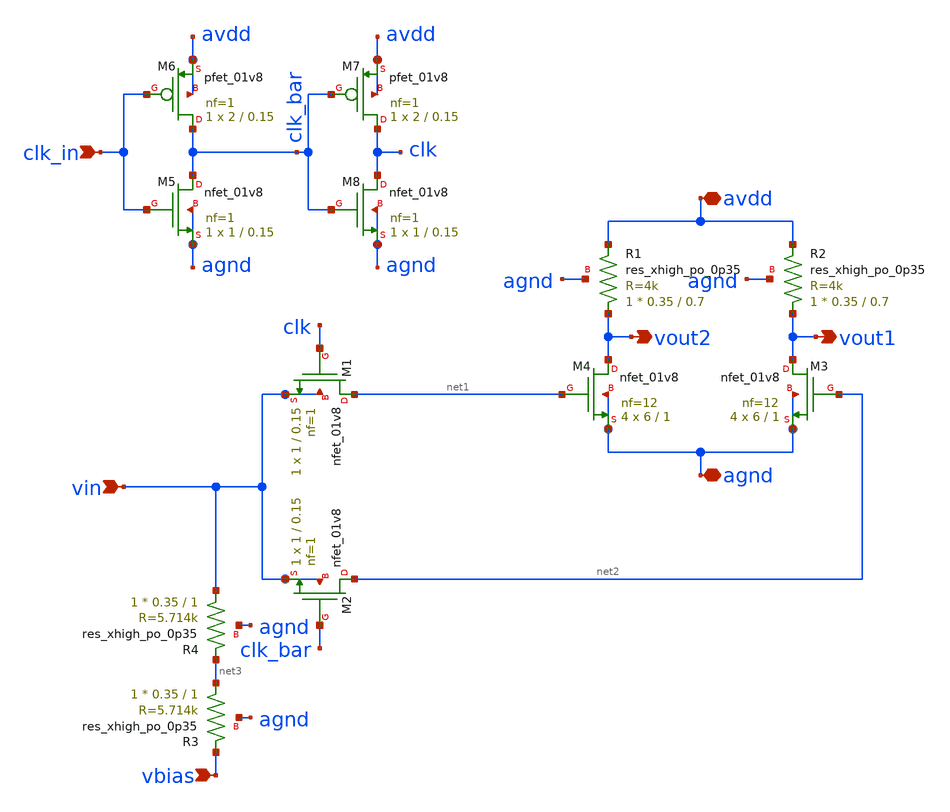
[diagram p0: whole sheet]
** sch_path: Mixer/Mixer.sch
**.subckt Mixer vin clk_in avdd agnd vout2 vout1 vbias
*.ipin vin
*.ipin clk_in
*.iopin avdd
*.iopin agnd
*.opin vout2
*.opin vout1
*.ipin vbias
XM1 net1 clk vin vin sky130_fd_pr__nfet_01v8 L=0.15 W=1 nf=1 ad='int((nf+1)/2) * W/nf * 0.29' as='int((nf+2)/2) * W/nf * 0.29'
+ pd='2*int((nf+1)/2) * (W/nf + 0.29)' ps='2*int((nf+2)/2) * (W/nf + 0.29)' nrd='0.29 / W' nrs='0.29 / W'
+ sa=0 sb=0 sd=0 mult=1 m=1
XM2 net2 clk_bar vin vin sky130_fd_pr__nfet_01v8 L=0.15 W=1 nf=1 ad='int((nf+1)/2) * W/nf * 0.29' as='int((nf+2)/2) * W/nf * 0.29'
+ pd='2*int((nf+1)/2) * (W/nf + 0.29)' ps='2*int((nf+2)/2) * (W/nf + 0.29)' nrd='0.29 / W' nrs='0.29 / W'
+ sa=0 sb=0 sd=0 mult=1 m=1
XM3 vout1 net2 agnd agnd sky130_fd_pr__nfet_01v8 L=1 W=6 nf=12 ad='int((nf+1)/2) * W/nf * 0.29' as='int((nf+2)/2) * W/nf * 0.29'
+ pd='2*int((nf+1)/2) * (W/nf + 0.29)' ps='2*int((nf+2)/2) * (W/nf + 0.29)' nrd='0.29 / W' nrs='0.29 / W'
+ sa=0 sb=0 sd=0 mult=4 m=4
XM4 vout2 net1 agnd agnd sky130_fd_pr__nfet_01v8 L=1 W=6 nf=12 ad='int((nf+1)/2) * W/nf * 0.29' as='int((nf+2)/2) * W/nf * 0.29'
+ pd='2*int((nf+1)/2) * (W/nf + 0.29)' ps='2*int((nf+2)/2) * (W/nf + 0.29)' nrd='0.29 / W' nrs='0.29 / W'
+ sa=0 sb=0 sd=0 mult=4 m=4
XR1 vout2 avdd agnd sky130_fd_pr__res_xhigh_po_0p35 L=0.7 mult=1 m=1
XR2 vout1 avdd agnd sky130_fd_pr__res_xhigh_po_0p35 L=0.7 mult=1 m=1
XR3 net3 vbias agnd sky130_fd_pr__res_xhigh_po_0p35 L=1 mult=1 m=1
XM6 clk_bar clk_in avdd avdd sky130_fd_pr__pfet_01v8 L=0.15 W=2 nf=1 ad='int((nf+1)/2) * W/nf * 0.29'
+ as='int((nf+2)/2) * W/nf * 0.29' pd='2*int((nf+1)/2) * (W/nf + 0.29)' ps='2*int((nf+2)/2) * (W/nf + 0.29)'
+ nrd='0.29 / W' nrs='0.29 / W' sa=0 sb=0 sd=0 mult=1 m=1
XM5 clk_bar clk_in agnd agnd sky130_fd_pr__nfet_01v8 L=0.15 W=1 nf=1 ad='int((nf+1)/2) * W/nf * 0.29'
+ as='int((nf+2)/2) * W/nf * 0.29' pd='2*int((nf+1)/2) * (W/nf + 0.29)' ps='2*int((nf+2)/2) * (W/nf + 0.29)'
+ nrd='0.29 / W' nrs='0.29 / W' sa=0 sb=0 sd=0 mult=1 m=1
XM7 clk clk_bar avdd avdd sky130_fd_pr__pfet_01v8 L=0.15 W=2 nf=1 ad='int((nf+1)/2) * W/nf * 0.29' as='int((nf+2)/2) * W/nf * 0.29'
+ pd='2*int((nf+1)/2) * (W/nf + 0.29)' ps='2*int((nf+2)/2) * (W/nf + 0.29)' nrd='0.29 / W' nrs='0.29 / W'
+ sa=0 sb=0 sd=0 mult=1 m=1
XM8 clk clk_bar agnd agnd sky130_fd_pr__nfet_01v8 L=0.15 W=1 nf=1 ad='int((nf+1)/2) * W/nf * 0.29' as='int((nf+2)/2) * W/nf * 0.29'
+ pd='2*int((nf+1)/2) * (W/nf + 0.29)' ps='2*int((nf+2)/2) * (W/nf + 0.29)' nrd='0.29 / W' nrs='0.29 / W'
+ sa=0 sb=0 sd=0 mult=1 m=1
XR4 vin net3 agnd sky130_fd_pr__res_xhigh_po_0p35 L=1 mult=1 m=1
**.ends
.end
